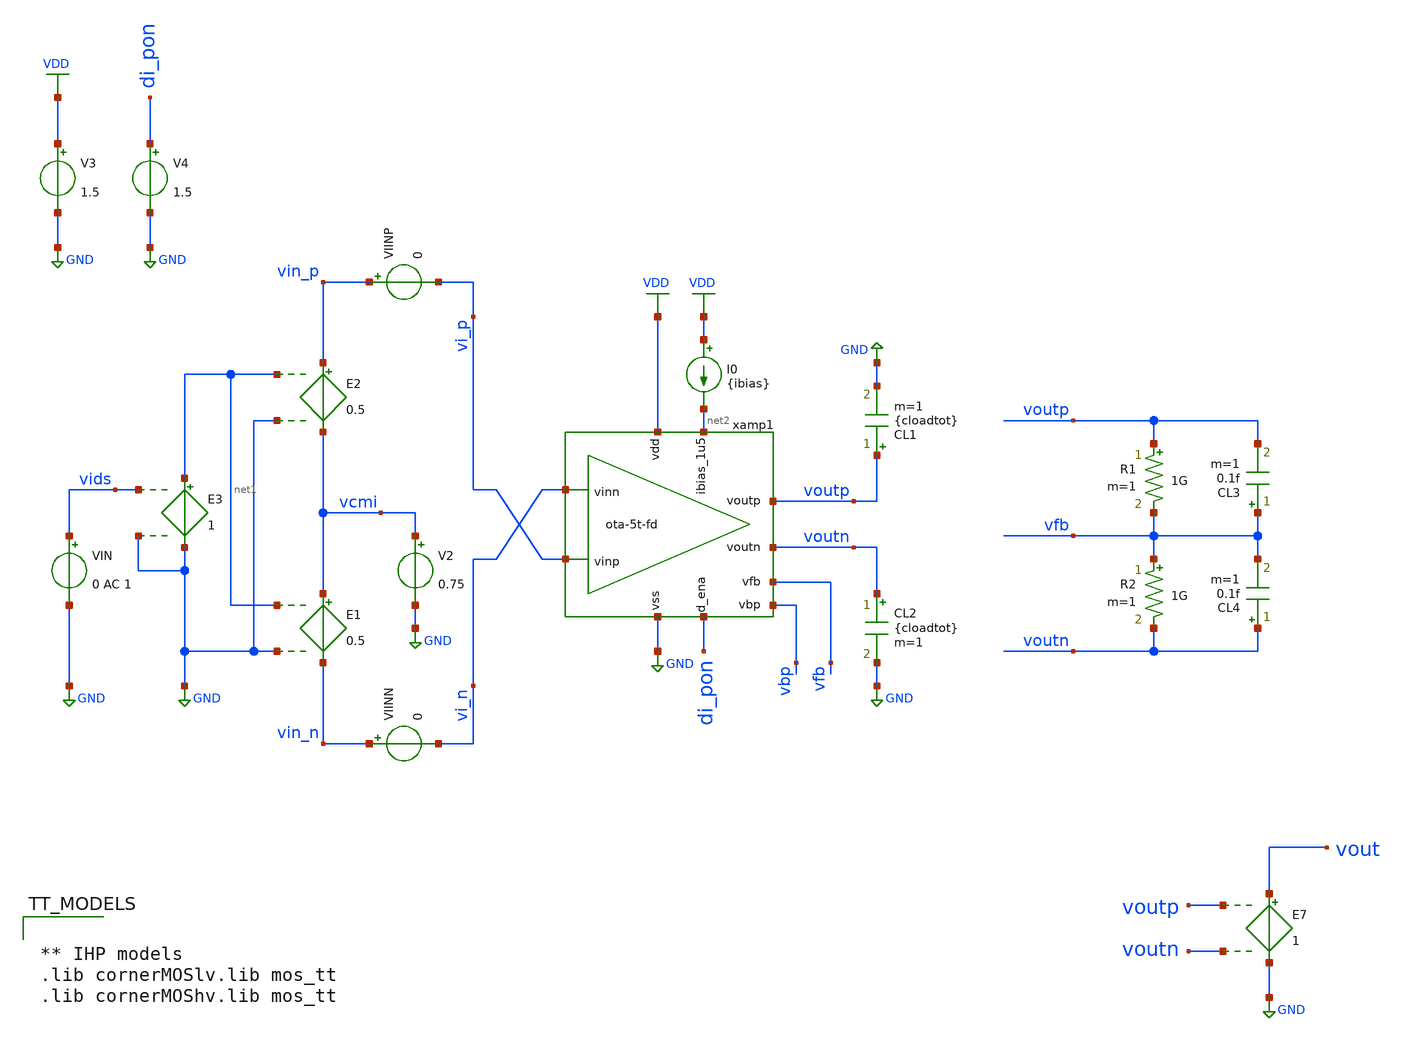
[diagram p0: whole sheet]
** sch_path: xschem/ota-5t-fd_tb-ol.sch
* xschem/ota-5t-fd.sch:
* (c) 2025 M. Koefinger
**.subckt ota-5t-fd_tb-ol
V3 VDD GND 1.5
V2 vcmi GND 0.75
E1 vcmi vin_n net1 GND 0.5
E2 vin_p vcmi net1 GND 0.5
VIN vids GND 0 AC 1
E3 net1 GND vids GND 1
VIINP vin_p vi_p 0
VIINN vin_n vi_n 0
V4 di_pon GND 1.5
E7 vout GND voutp voutn 1
CL2 voutn GND {cloadtot} m=1
CL1 voutp GND {cloadtot} m=1
I0 VDD net2 {ibias}
R1 voutp vfb 1G m=1
R2 vfb voutn 1G m=1
CL3 vfb voutp 0.1f m=1
CL4 voutn vfb 0.1f m=1
xamp1 VDD vfb voutp voutn vi_p vi_n net2 di_pon GND vbp ota-5t-fd
**** begin user architecture code


*.include /foss/designs/xschem/ota-5t-fd-dev-sav.spice
.include ota-5t-fd_tb-ol.save
.options savecurrents
.param ibias=300n
.param ci=100f
.param cload=2*ci
.param cf=ci
.param beta=0.5
.param cloadtot=cload+(1-beta)*cf

.save all
.control
set doAmpSim = 1

if $doAmpSim eq 1
	setplot const
	let f_min = 10
	let f_max = 1G
	let f_stop = 500k

	let Adc = 16
	let v_step_o = 1
	let v_step_i = -v_step_o/Adc

	let t_rf = 0.01u
	let t_step = 100u
	let t_delay = 0
	let t_per = 2*t_step

	let tstep = 0.001*t_step
	let tstop = 2*t_per
	let tstart = t_delay

	alter @VIN[DC] = 0.0
	alter @VIN[PULSE] = [ 0 $&v_step_i $&t_delay $&t_rf $&t_rf $&t_step $&t_per 0 ]

	ac dec 100 $&const.f_min $&const.f_max
	noise v(vout) vin dec 100 $&const.f_min $&const.f_max
	tran $&tstep $&tstop $&tstart

	setplot ac1
	let Atot = v(vout)/v(vids)
	let Amag_ol_dB = vdb(Atot)
	let Aarg_ol = 180/PI*cphase(Atot)
	meas ac Adc_ol_dB max Amag_ol_dB
	let Amag_fc = Adc_ol_dB-3
	meas ac fc find frequency when Amag_ol_dB = Amag_fc
	meas ac fug_ol find frequency when Amag_ol_dB=0
	meas ac pm find Aarg_ol when frequency=fug_ol
	let pm = 180 + pm
	print pm
	let Adc_ol_lin = 10^(Adc_ol_dB/20)
	let err_gain = 1-Adc_ol_lin/(1+Adc_ol_lin)
	print err_gain*100
	plot Amag_ol_dB Aarg_ol ylabel 'Open Loop Magnitude, Phase'

	setplot noise1
	let acgain = onoise_spectrum/inoise_spectrum
	plot onoise_spectrum ylog xlog ylabel 'Output Noise'
	*plot acgain

	setplot noise2
	print onoise_total

	setplot tran2
	let vcmo = (v(voutp)+v(voutn))/2
	plot v(vin_p) v(vin_n) v(voutp) v(voutn) vcmo
end

reset
op
let gmId_load = @n.xamp1.xmp1.nsg13_lv_pmos[gm]/@n.xamp1.xmp1.nsg13_lv_pmos[ids]
let gmId_active = @n.xamp1.xmn1.nsg13_lv_nmos[gm]/@n.xamp1.xmn1.nsg13_lv_nmos[ids]
print gmId_load
print gmId_active
remzerovec
write ota-5t-fd_tb-ol.raw
.endc



** IHP models
.lib cornerMOSlv.lib mos_tt
.lib cornerMOShv.lib mos_tt


**** end user architecture code
**.ends

* expanding   symbol:  ota-5t-fd.sym # of pins=10
** sym_path: xschem/ota-5t-fd.sym
** sch_path: xschem/ota-5t-fd.sch
.subckt ota-5t-fd vdd vfb voutp voutn vinp vinn ibias_1u5 d_ena vss vbp
*.ipin ibias_1u5
*.iopin vdd
*.iopin vss
*.ipin vinp
*.ipin vinn
*.opin voutn
*.ipin d_ena
*.opin voutp
*.ipin vfb
*.opin vbp
XMN3 tail gate_n vss vss sg13_lv_nmos w=2.5u l=0.5u ng=5 m=1 mm_ok=1
XMP2 voutp vfb vdd vdd sg13_lv_pmos w=0.5u l=0.5u ng=1 m=1 mm_ok=1
XMN1 voutn vinp tail vss sg13_lv_nmos w=5.5u l=0.5u ng=11 m=1 mm_ok=1
XMN2 voutp vinn tail vss sg13_lv_nmos w=5.5u l=0.5u ng=11 m=1 mm_ok=1
XMP1 voutn vfb vdd vdd sg13_lv_pmos w=0.5u l=0.5u ng=1 m=1 mm_ok=1
XMN4 ibias_1u5 gate_n vss vss sg13_lv_nmos w=1.5u l=0.5u ng=3 m=1 mm_ok=1
XMN5 gate_n ena_n vss vss sg13_lv_nmos w=0.5u l=0.13u ng=1 m=1 mm_ok=1
XMPSW1 vfb ena vdd vdd sg13_lv_pmos w=1.5u l=0.13u ng=1 m=1 mm_ok=1
XMN8 ena ena_n vss vss sg13_lv_nmos w=0.5u l=0.13u ng=1 m=1 mm_ok=1
XMP5 ena ena_n vdd vdd sg13_lv_pmos w=1.5u l=0.13u ng=1 m=1 mm_ok=1
XMN6 ibias_1u5 ena gate_n vss sg13_lv_nmos w=0.5u l=0.13u ng=1 m=1 mm_ok=1
XMN7 ena_n d_ena vss vss sg13_lv_nmos w=0.5u l=0.13u ng=1 m=1 mm_ok=1
XMP4 ena_n d_ena vdd vdd sg13_lv_pmos w=1.5u l=0.13u ng=1 m=1 mm_ok=1
XMN9 vbp gate_n vss vss sg13_lv_nmos w=1u l=0.5u ng=2 m=1 mm_ok=1
XMP3 vbp vbp vdd vdd sg13_lv_pmos w=0.5u l=0.5u ng=1 m=1 mm_ok=1
.ends

.GLOBAL GND
.GLOBAL VDD
.end
